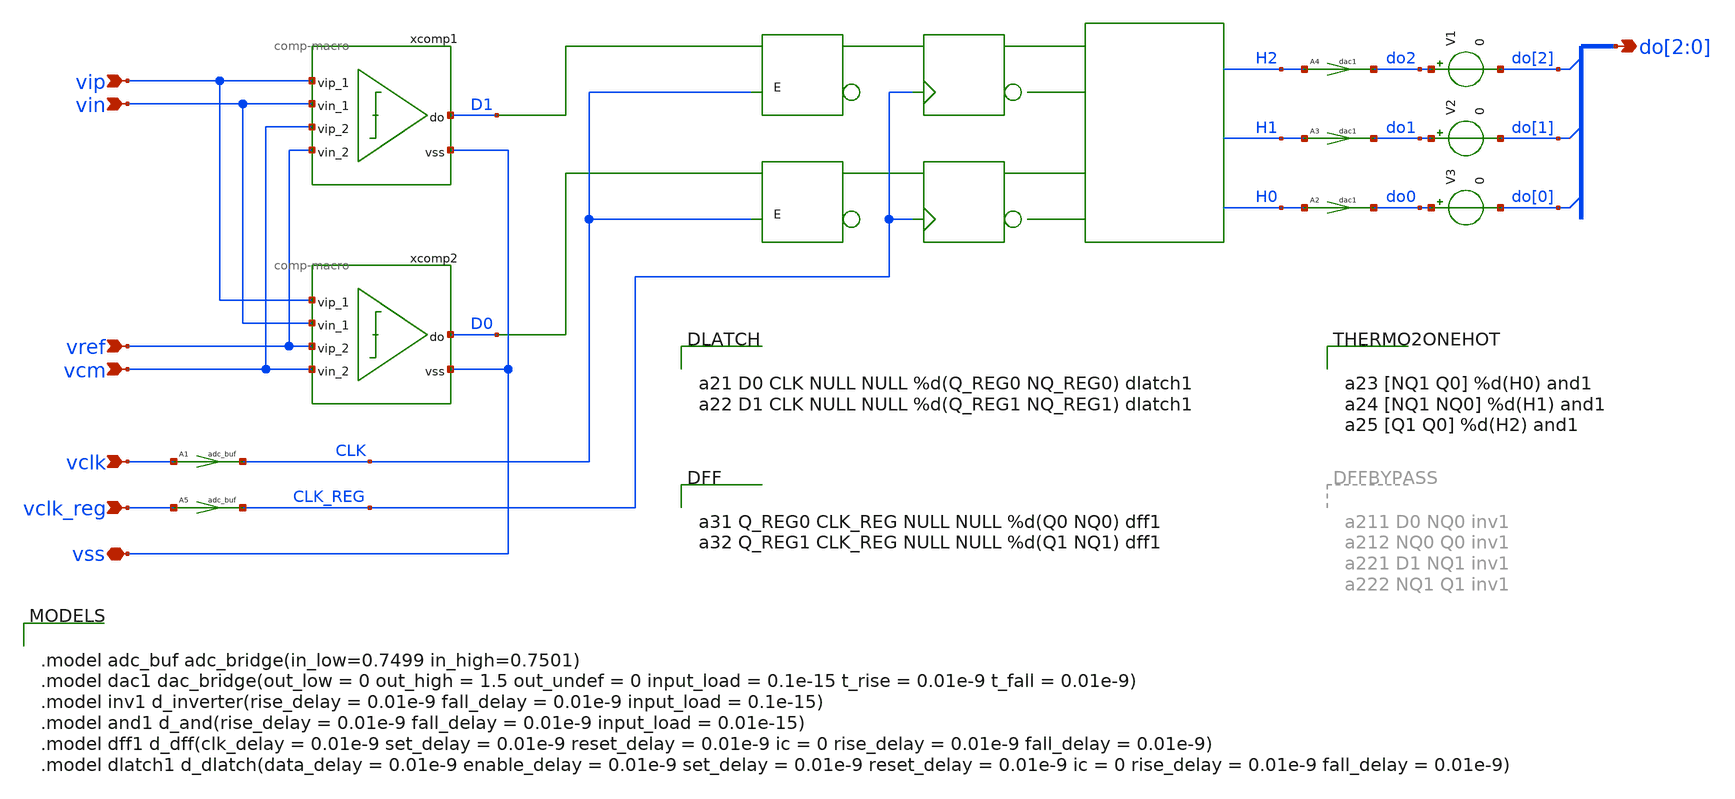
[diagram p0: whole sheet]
** sch_path: xschem/adc-tri-lvl-ideal.sch
**.subckt adc-tri-lvl-ideal vss vip vin vref vcm vclk do[2],do[1],do[0] vclk_reg
*.iopin vss
*.ipin vip
*.ipin vin
*.ipin vref
*.ipin vcm
*.ipin vclk
*.opin do[2],do[1],do[0]
*.ipin vclk_reg
xcomp1 D1 vip vin vcm vref vss comp-macro
xcomp2 D0 vip vin vref vcm vss comp-macro
A1 [ vclk ] [ CLK ] adc_buf
A3 [ H1 ] [ do1 ] dac1
A4 [ H2 ] [ do2 ] dac1
A2 [ H0 ] [ do0 ] dac1
V1 do2 do[2] 0
V2 do1 do[1] 0
V3 do0 do[0] 0
A5 [ vclk_reg ] [ CLK_REG ] adc_buf
**.ends

* expanding   symbol:  comp-macro.sym # of pins=6
** sym_path: xschem/comp-macro.sym
** sch_path: xschem/comp-macro.sch
.subckt comp-macro do vip_1 vin_1 vip_2 vin_2 vss
*.iopin vss
*.ipin vip_1
*.ipin vin_1
*.ipin vip_2
*.ipin vin_2
*.opin do
A1 [ net1 ] [ do ] comp0
E1 net1 net2 vip_1 vin_1 1
E2 net2 vss vip_2 vin_2 1
**** begin user architecture code

.model comp0 adc_bridge(in_low=-0.0001 in_high=0.0001)

**** end user architecture code
.ends

**** begin user architecture code


a31 Q_REG0 CLK_REG NULL NULL %d(Q0 NQ0) dff1
a32 Q_REG1 CLK_REG NULL NULL %d(Q1 NQ1) dff1




.model adc_buf adc_bridge(in_low=0.7499 in_high=0.7501)
.model dac1 dac_bridge(out_low = 0 out_high = 1.5 out_undef = 0 input_load = 0.1e-15 t_rise =
+ 0.01e-9 t_fall = 0.01e-9)
.model inv1 d_inverter(rise_delay = 0.01e-9 fall_delay = 0.01e-9 input_load = 0.1e-15)
.model and1 d_and(rise_delay = 0.01e-9 fall_delay = 0.01e-9 input_load = 0.01e-15)
.model dff1 d_dff(clk_delay = 0.01e-9 set_delay = 0.01e-9 reset_delay = 0.01e-9 ic = 0 rise_delay =
+ 0.01e-9 fall_delay = 0.01e-9)
.model dlatch1 d_dlatch(data_delay = 0.01e-9 enable_delay = 0.01e-9 set_delay = 0.01e-9 reset_delay
+ = 0.01e-9 ic = 0 rise_delay = 0.01e-9 fall_delay = 0.01e-9)



a23 [NQ1 Q0] %d(H0) and1
a24 [NQ1 NQ0] %d(H1) and1
a25 [Q1 Q0] %d(H2) and1




a21 D0 CLK NULL NULL %d(Q_REG0 NQ_REG0) dlatch1
a22 D1 CLK NULL NULL %d(Q_REG1 NQ_REG1) dlatch1


**** end user architecture code
.end
